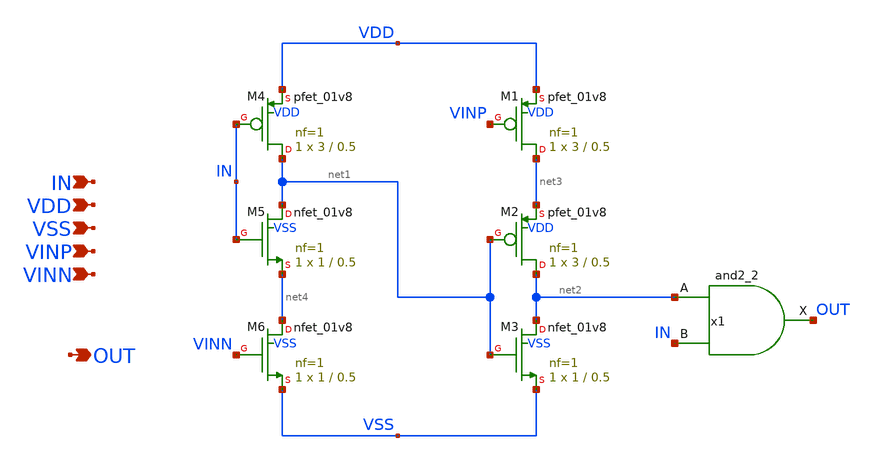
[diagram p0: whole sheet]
** sch_path: xschem/delay_gate_ori.sch
**.subckt delay_gate_ori VINP VINN IN VSS VDD OUT
*.ipin VINP
*.ipin VINN
*.ipin IN
*.ipin VSS
*.ipin VDD
*.opin OUT
XM1 net3 VINP VDD VDD sky130_fd_pr__pfet_01v8 L=0.5 W=3 nf=1 ad='int((nf+1)/2) * W/nf * 0.29' as='int((nf+2)/2) * W/nf * 0.29'
+ pd='2*int((nf+1)/2) * (W/nf + 0.29)' ps='2*int((nf+2)/2) * (W/nf + 0.29)' nrd='0.29 / W' nrs='0.29 / W'
+ sa=0 sb=0 sd=0 mult=1 m=1
XM2 net2 net1 net3 VDD sky130_fd_pr__pfet_01v8 L=0.5 W=3 nf=1 ad='int((nf+1)/2) * W/nf * 0.29' as='int((nf+2)/2) * W/nf * 0.29'
+ pd='2*int((nf+1)/2) * (W/nf + 0.29)' ps='2*int((nf+2)/2) * (W/nf + 0.29)' nrd='0.29 / W' nrs='0.29 / W'
+ sa=0 sb=0 sd=0 mult=1 m=1
XM3 net2 net1 VSS VSS sky130_fd_pr__nfet_01v8 L=0.5 W=1 nf=1 ad='int((nf+1)/2) * W/nf * 0.29' as='int((nf+2)/2) * W/nf * 0.29'
+ pd='2*int((nf+1)/2) * (W/nf + 0.29)' ps='2*int((nf+2)/2) * (W/nf + 0.29)' nrd='0.29 / W' nrs='0.29 / W'
+ sa=0 sb=0 sd=0 mult=1 m=1
XM4 net1 IN VDD VDD sky130_fd_pr__pfet_01v8 L=0.5 W=3 nf=1 ad='int((nf+1)/2) * W/nf * 0.29' as='int((nf+2)/2) * W/nf * 0.29'
+ pd='2*int((nf+1)/2) * (W/nf + 0.29)' ps='2*int((nf+2)/2) * (W/nf + 0.29)' nrd='0.29 / W' nrs='0.29 / W'
+ sa=0 sb=0 sd=0 mult=1 m=1
XM5 net1 IN net4 VSS sky130_fd_pr__nfet_01v8 L=0.5 W=1 nf=1 ad='int((nf+1)/2) * W/nf * 0.29' as='int((nf+2)/2) * W/nf * 0.29'
+ pd='2*int((nf+1)/2) * (W/nf + 0.29)' ps='2*int((nf+2)/2) * (W/nf + 0.29)' nrd='0.29 / W' nrs='0.29 / W'
+ sa=0 sb=0 sd=0 mult=1 m=1
XM6 net4 VINN VSS VSS sky130_fd_pr__nfet_01v8 L=0.5 W=1 nf=1 ad='int((nf+1)/2) * W/nf * 0.29' as='int((nf+2)/2) * W/nf * 0.29'
+ pd='2*int((nf+1)/2) * (W/nf + 0.29)' ps='2*int((nf+2)/2) * (W/nf + 0.29)' nrd='0.29 / W' nrs='0.29 / W'
+ sa=0 sb=0 sd=0 mult=1 m=1
x1 net2 IN VSS VSS VDD VDD OUT sky130_fd_sc_hd__and2_2
**.ends
.end
